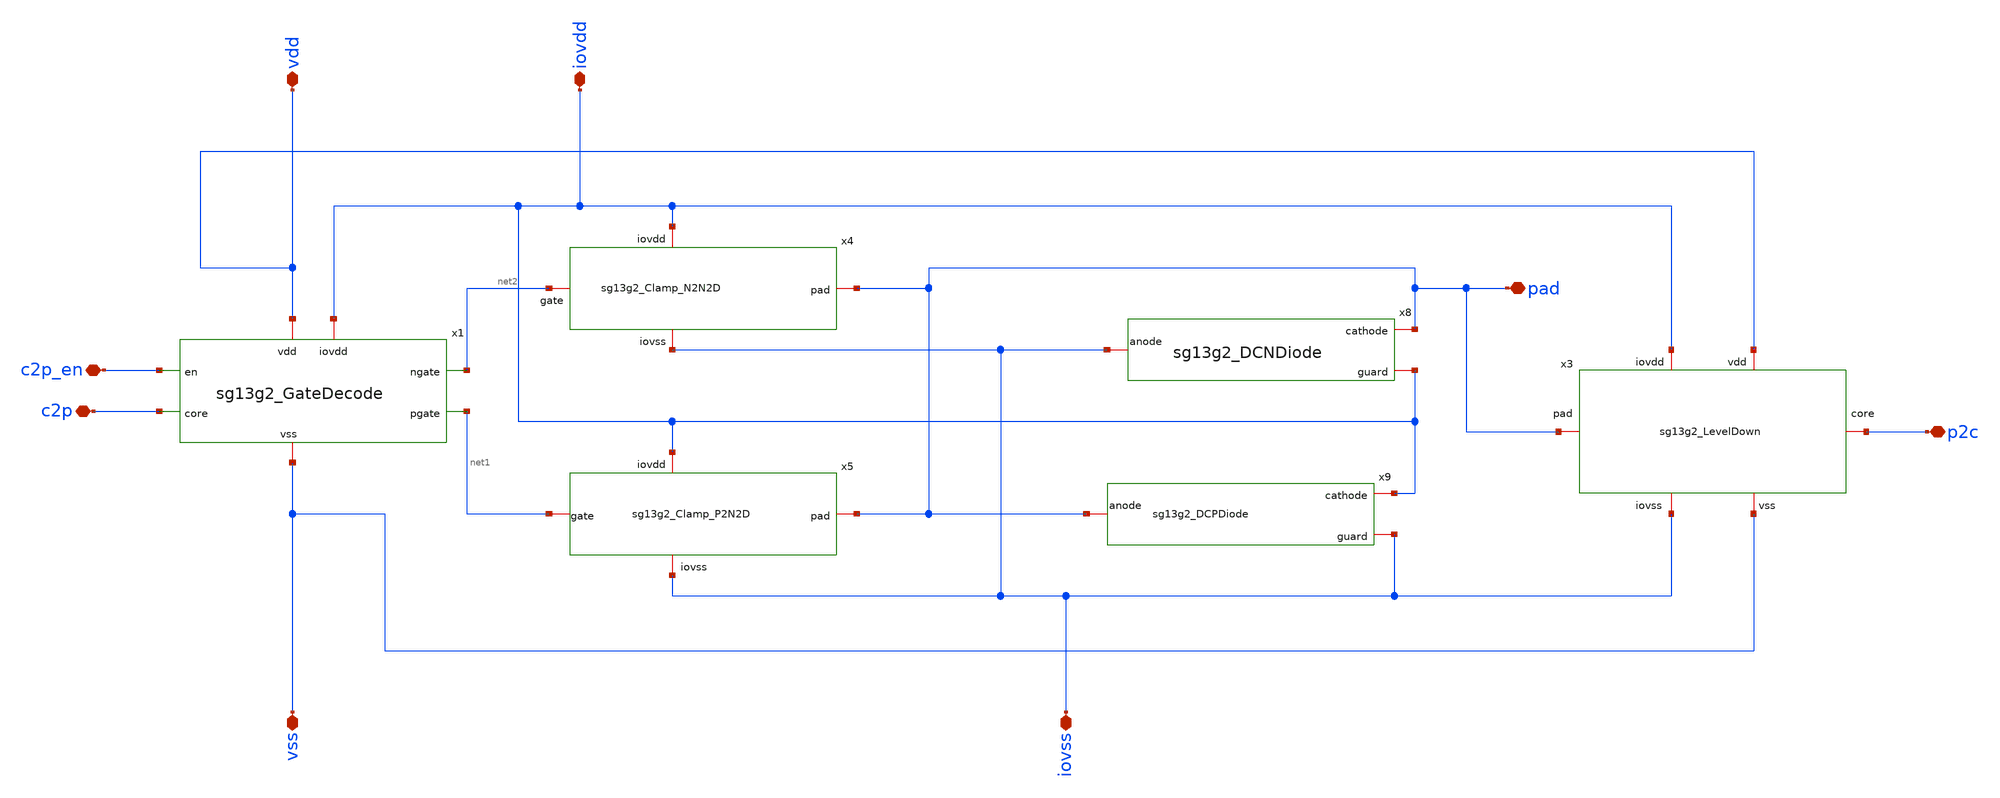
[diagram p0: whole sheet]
** sch_path: CDR4176-main/schematic/xschem/project_io/sg13g2_IOPadInOut4mA/sg13g2_IOPadInOut4mA.sch
**.subckt sg13g2_IOPadInOut4mA iovss pad vss c2p vdd iovdd c2p_en p2c
*.iopin iovss
*.iopin pad
*.iopin vss
*.iopin c2p
*.iopin vdd
*.iopin iovdd
*.iopin c2p_en
*.iopin p2c
x8 pad iovss iovdd sg13g2_DCNDiode
x9 iovdd pad iovss sg13g2_DCPDiode
x4 iovdd pad net2 iovss sg13g2_Clamp_N2N2D
x5 iovdd net1 iovss pad sg13g2_Clamp_P2N2D
x1 vdd iovdd c2p_en net2 net1 c2p vss sg13g2_GateDecode
x3 vdd iovdd p2c pad iovss vss sg13g2_LevelDown
**.ends
.end
